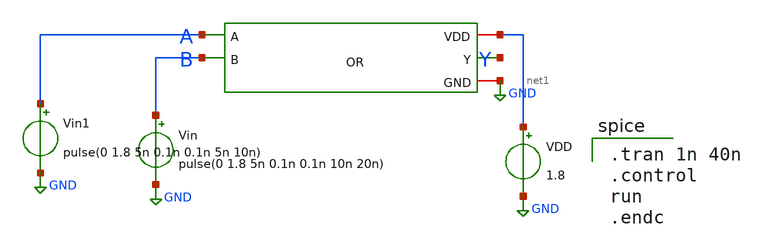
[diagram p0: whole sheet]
** sch_path: OR/OR_Testbench.sch
**.subckt OR_Testbench
x1 net1 A Y B GND OR
Vin1 A GND pulse(0 1.8 5n 0.1n 0.1n 5n 10n)
Vin B GND pulse(0 1.8 5n 0.1n 0.1n 10n 20n)
VDD net1 GND 1.8
**** begin user architecture code

.lib /usr/local/share/pdk/sky130A/libs.tech/ngspice/sky130.lib.spice tt


.tran 1n 40n
.control
run
.endc

**** end user architecture code
**.ends
.GLOBAL GND
.end
